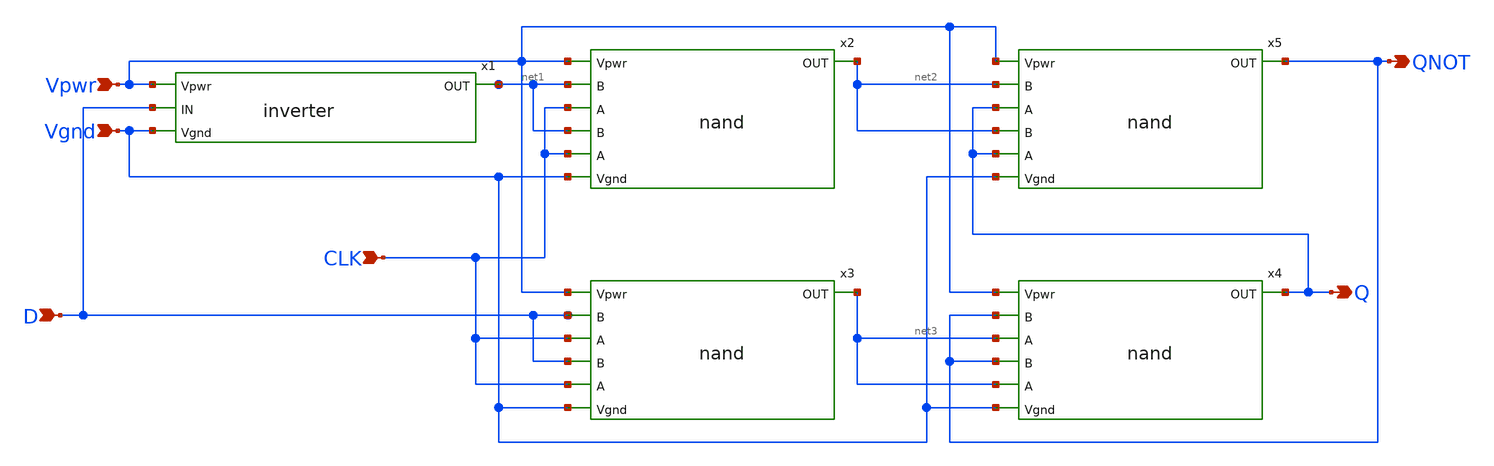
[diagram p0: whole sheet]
** sch_path: MUXDFF/Gates/DFF/dff.sch
**.subckt dff Vpwr D Vgnd CLK QNOT Q
*.ipin Vpwr
*.ipin D
*.ipin Vgnd
*.ipin CLK
*.opin QNOT
*.opin Q
x1 Vpwr D net1 Vgnd inverter
x2 Vpwr net1 CLK net2 Vgnd nand
x3 Vpwr D CLK net3 Vgnd nand
x4 Vpwr QNOT net3 Q Vgnd nand
x5 Vpwr net2 Q QNOT Vgnd nand
**.ends
.end
